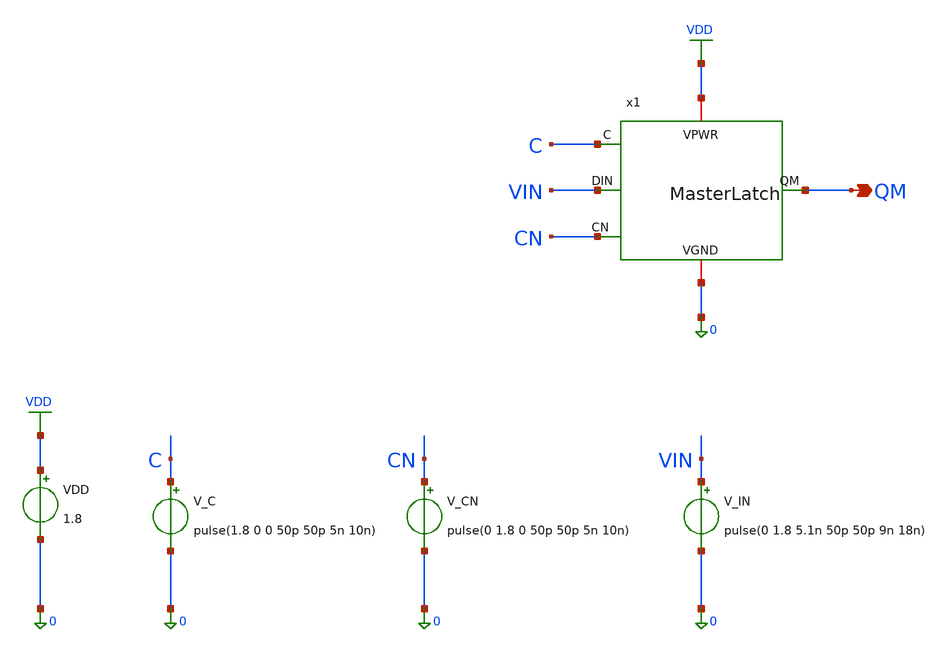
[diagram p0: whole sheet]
** sch_path: latch/MasterLatch_tb.sch
**.subckt MasterLatch_tb QM
*.opin QM
VDD VDD 0 1.8
V_C C 0 pulse(1.8 0 0 50p 50p 5n 10n)
V_CN CN 0 pulse(0 1.8 0 50p 50p 5n 10n)
V_IN VIN 0 pulse(0 1.8 5.1n 50p 50p 9n 18n)
x1 VIN QM C CN VDD 0 MasterLatch
**** begin user architecture code

** opencircuitdesign pdks install
.lib $::SKYWATER_MODELS/sky130.lib.spice tt



.tran 0.001n 11n
.control
  save all
    run
	meas tran delay TRIG v(C) VAL=0.9 RISE=1 TARG v(QM) VAL=0.9 RISE=1
	write /home/sushanth/.xschem/simulations/output.raw
  end
.endc


**** end user architecture code
**.ends
.GLOBAL VDD
.end
